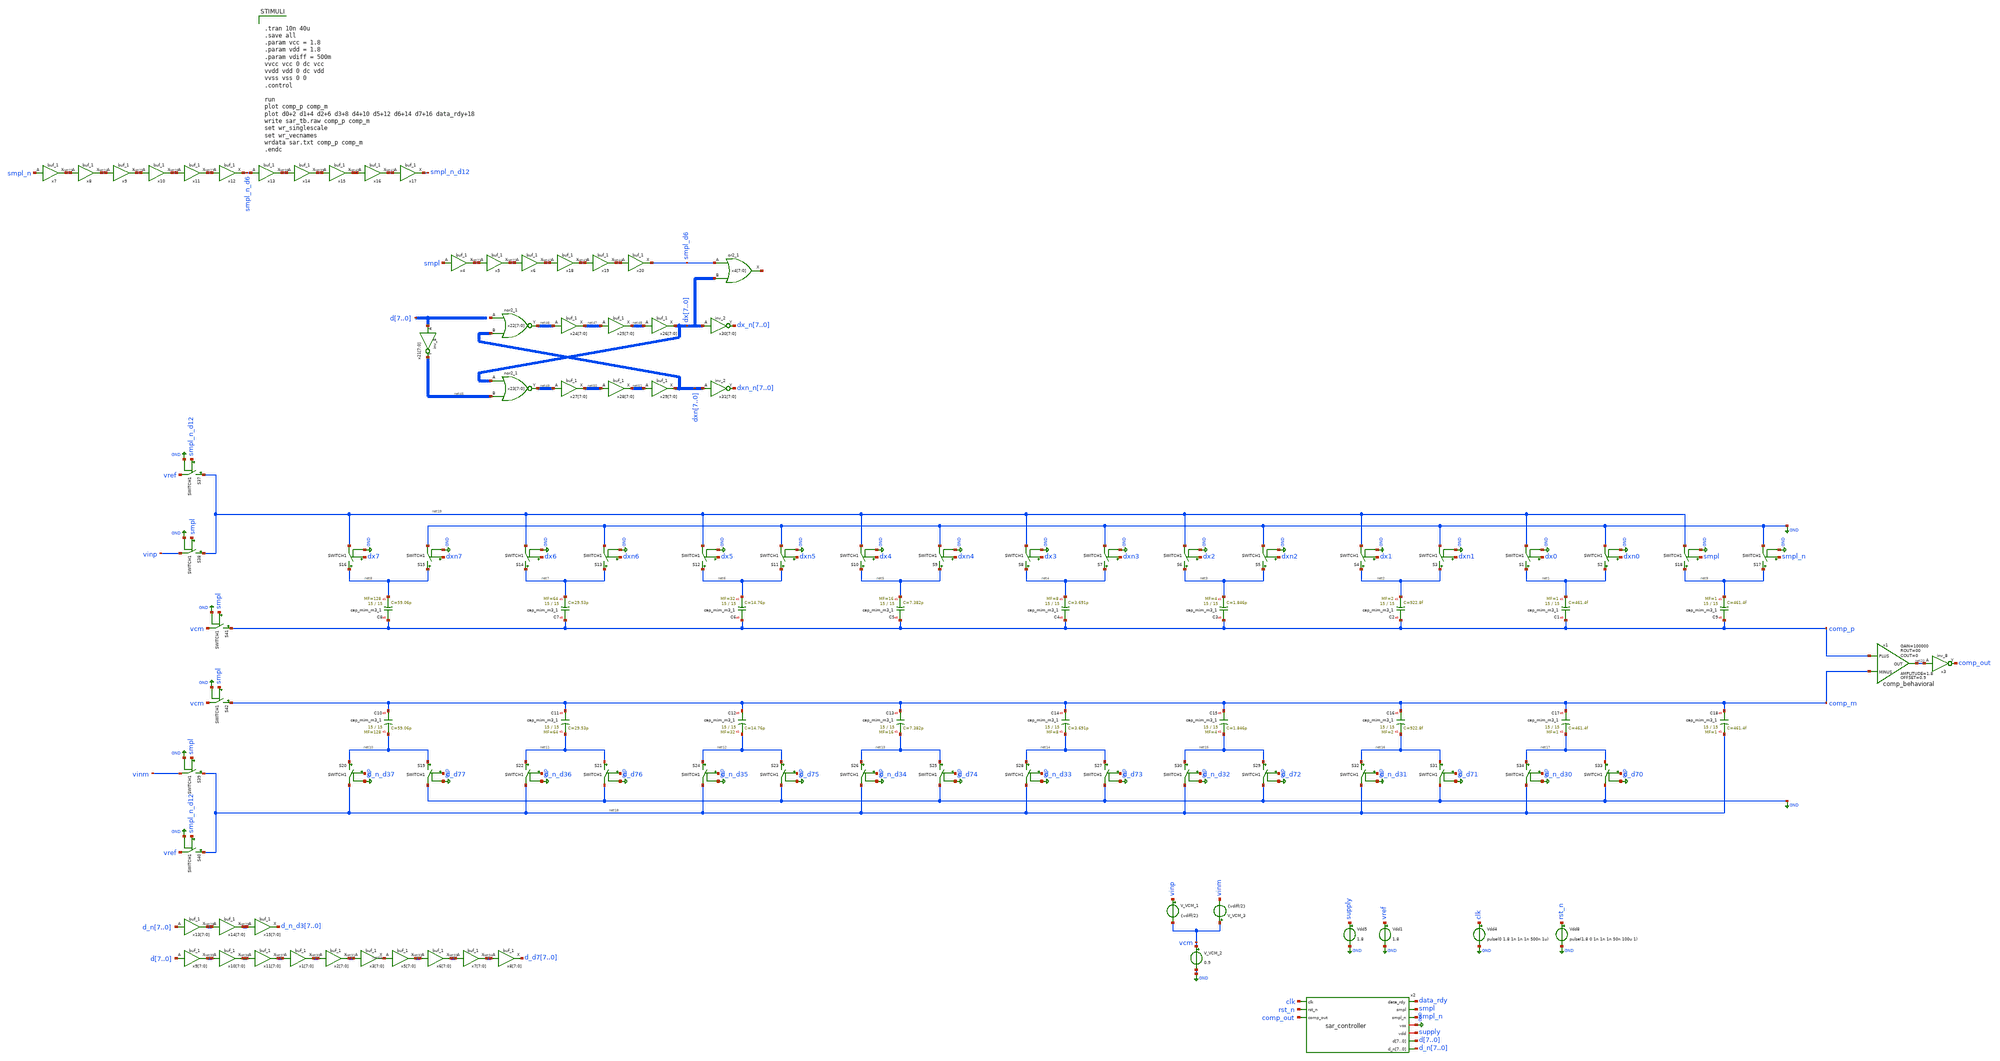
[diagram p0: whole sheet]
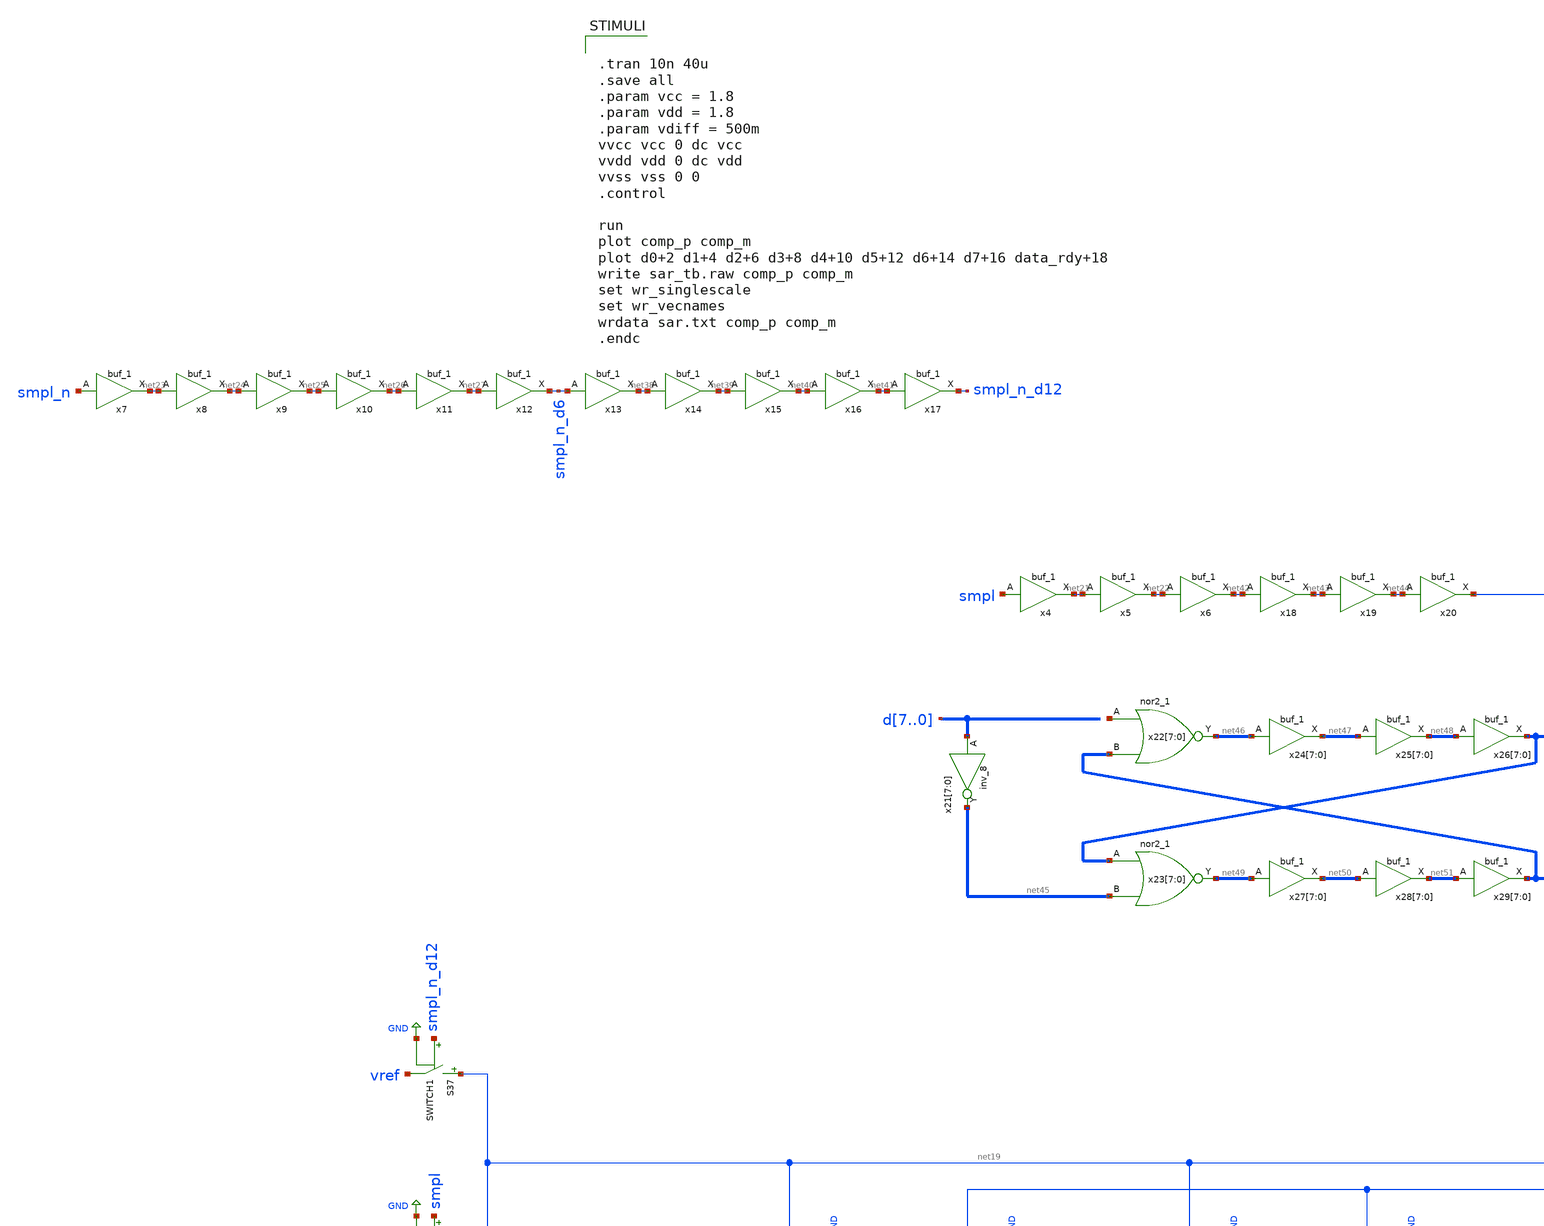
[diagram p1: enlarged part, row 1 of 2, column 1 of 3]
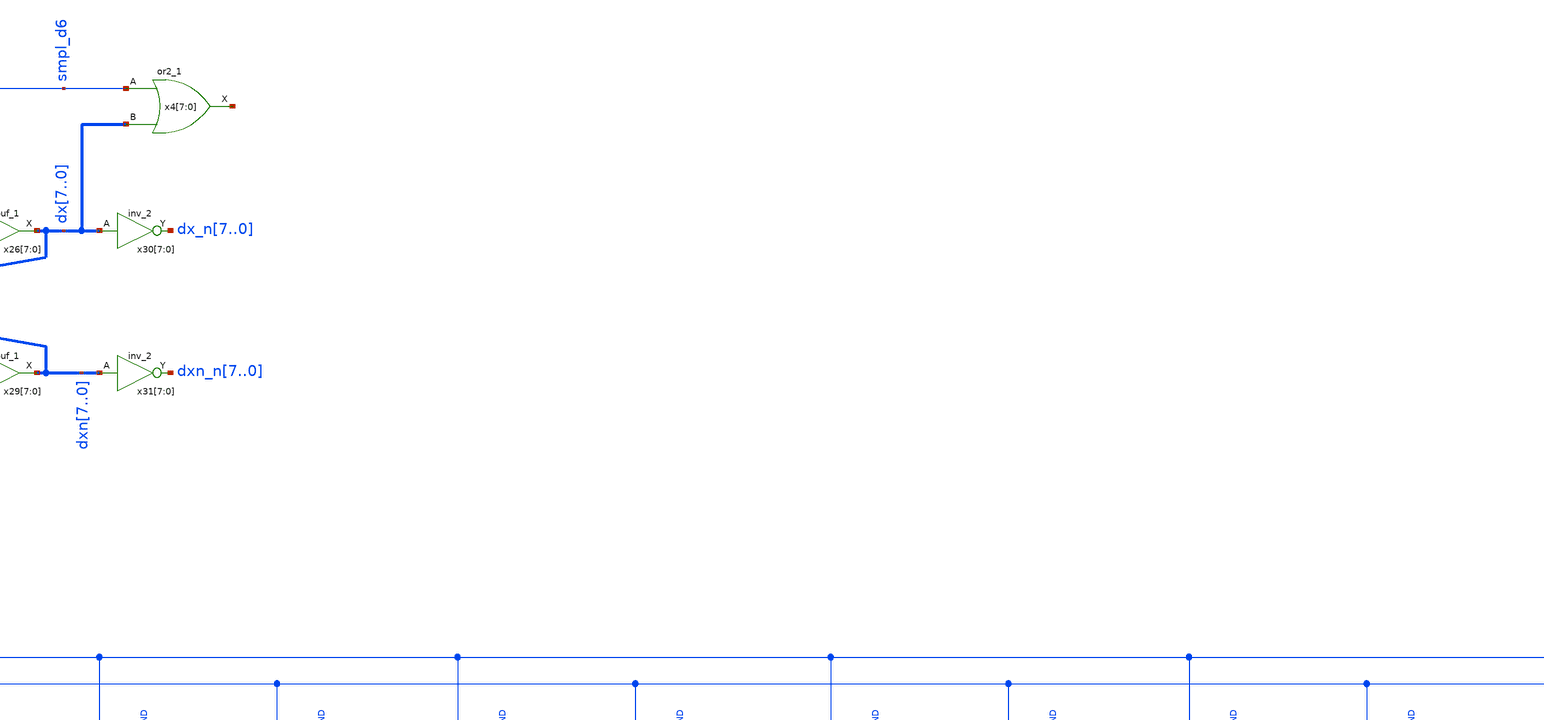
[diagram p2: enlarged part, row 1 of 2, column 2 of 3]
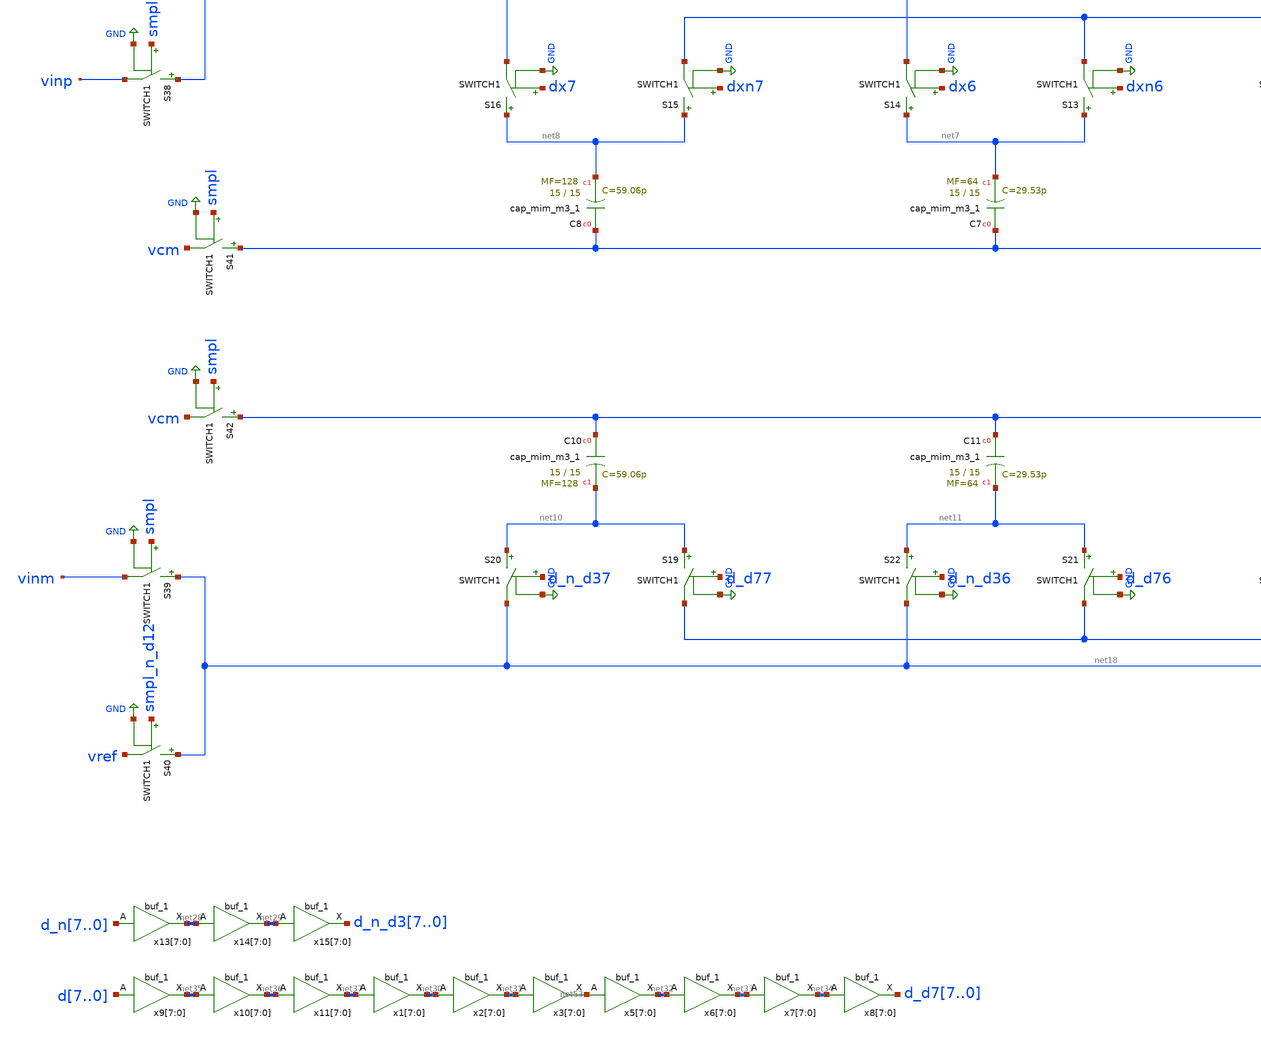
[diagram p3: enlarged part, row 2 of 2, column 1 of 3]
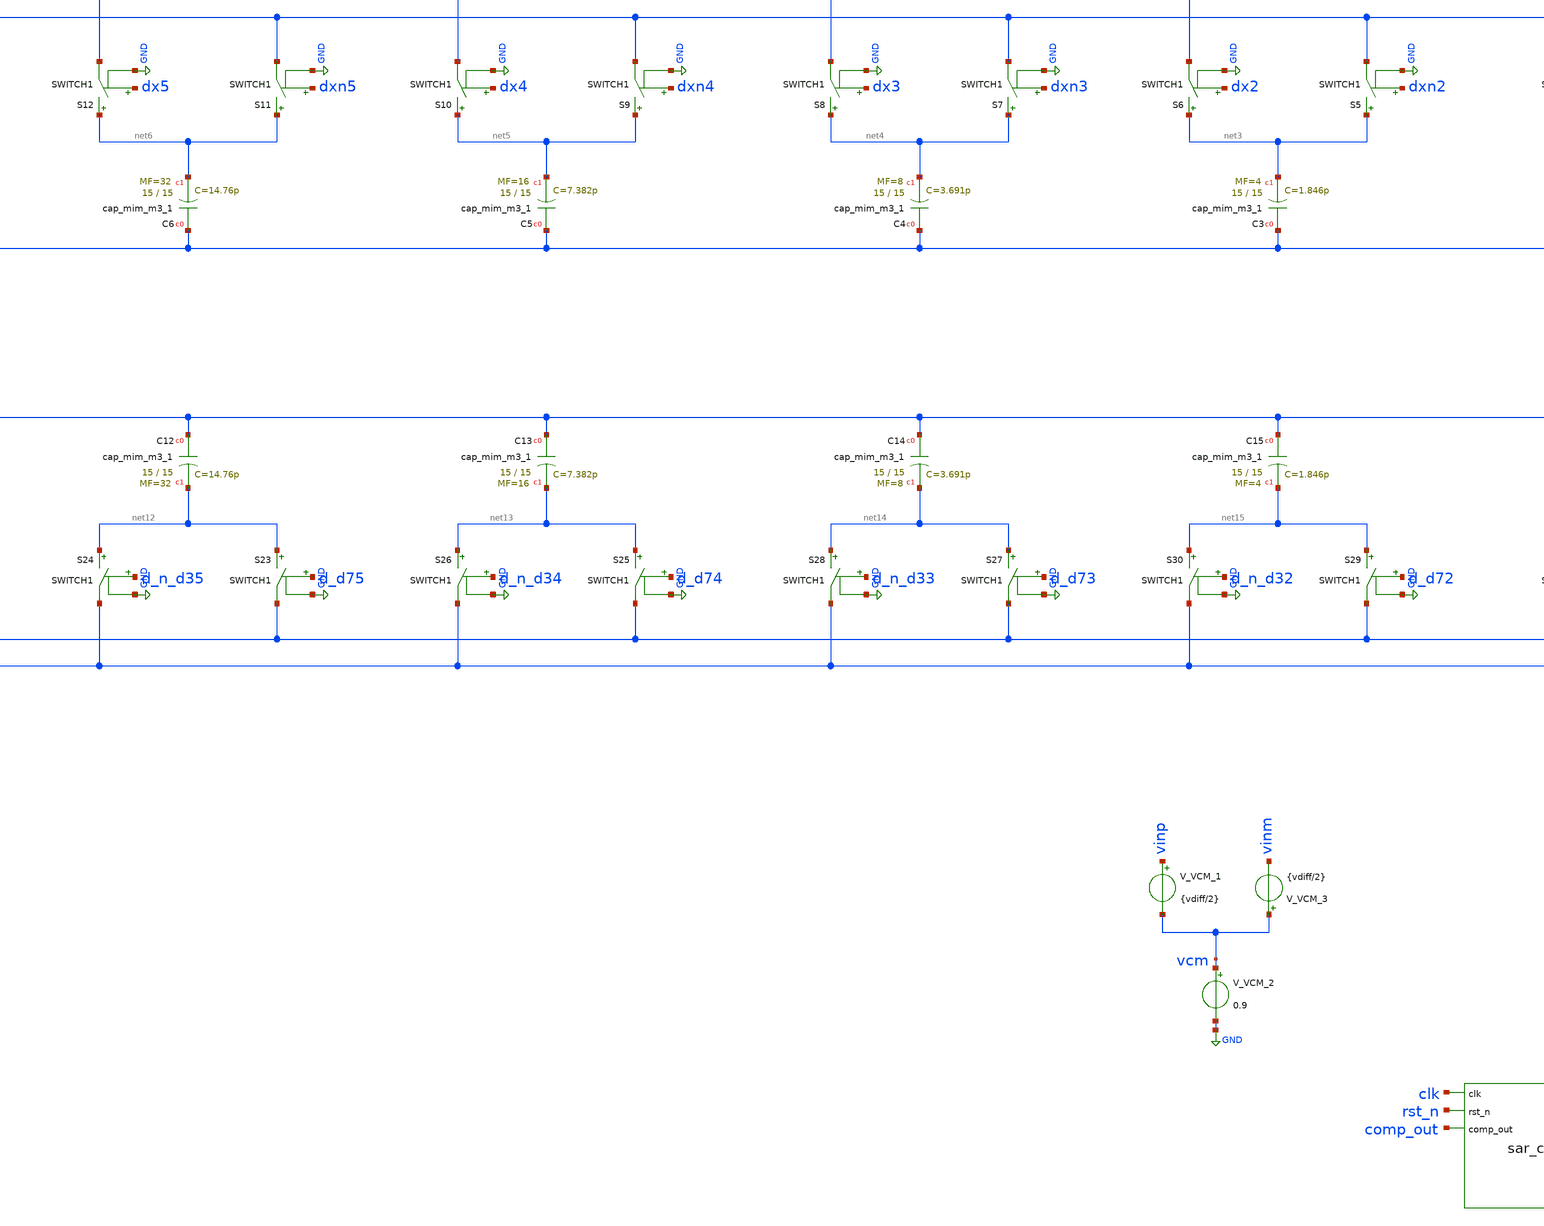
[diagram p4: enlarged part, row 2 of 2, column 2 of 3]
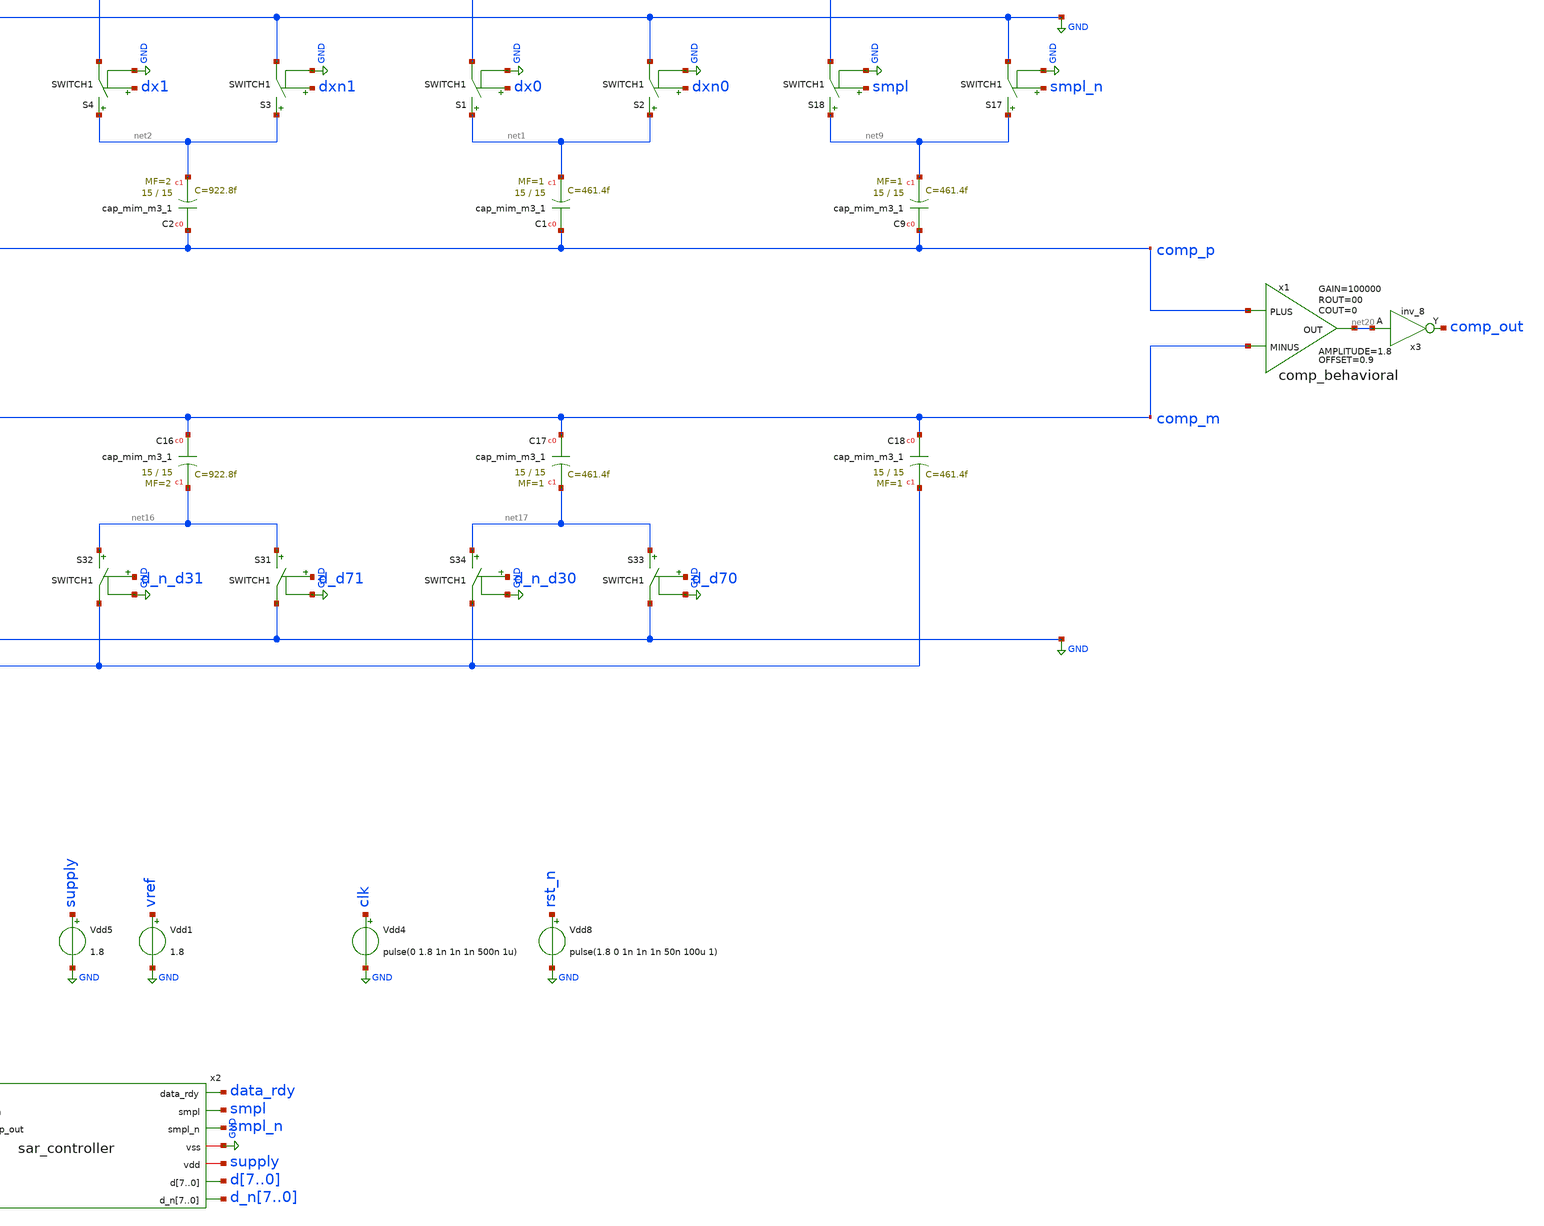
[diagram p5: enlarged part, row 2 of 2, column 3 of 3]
** sch_path: top/untitled-4.sch
.lib $::SKYWATER_MODELS/sky130.lib.spice tt
.include $::SKYWATER_STDCELLS/sky130_fd_sc_hd.spice

**.subckt untitled-4
XC1 comp_p net1 sky130_fd_pr__cap_mim_m3_1 W=15 L=15 MF=1 m=1
S2 net1 GND dxn0 GND SWITCH1
S1 net1 net19 dx0 GND SWITCH1
XC2 comp_p net2 sky130_fd_pr__cap_mim_m3_1 W=15 L=15 MF=2 m=2
S3 net2 GND dxn1 GND SWITCH1
S4 net2 net19 dx1 GND SWITCH1
XC3 comp_p net3 sky130_fd_pr__cap_mim_m3_1 W=15 L=15 MF=4 m=4
S5 net3 GND dxn2 GND SWITCH1
S6 net3 net19 dx2 GND SWITCH1
XC4 comp_p net4 sky130_fd_pr__cap_mim_m3_1 W=15 L=15 MF=8 m=8
S7 net4 GND dxn3 GND SWITCH1
S8 net4 net19 dx3 GND SWITCH1
XC5 comp_p net5 sky130_fd_pr__cap_mim_m3_1 W=15 L=15 MF=16 m=16
S9 net5 GND dxn4 GND SWITCH1
S10 net5 net19 dx4 GND SWITCH1
XC6 comp_p net6 sky130_fd_pr__cap_mim_m3_1 W=15 L=15 MF=32 m=32
S11 net6 GND dxn5 GND SWITCH1
S12 net6 net19 dx5 GND SWITCH1
XC7 comp_p net7 sky130_fd_pr__cap_mim_m3_1 W=15 L=15 MF=64 m=64
S13 net7 GND dxn6 GND SWITCH1
S14 net7 net19 dx6 GND SWITCH1
S15 net8 GND dxn7 GND SWITCH1
S16 net8 net19 dx7 GND SWITCH1
XC9 comp_p net9 sky130_fd_pr__cap_mim_m3_1 W=15 L=15 MF=1 m=1
S17 net9 GND smpl_n GND SWITCH1
S18 net9 net19 smpl GND SWITCH1
XC10 comp_m net10 sky130_fd_pr__cap_mim_m3_1 W=15 L=15 MF=128 m=128
S19 net10 GND d_d77 GND SWITCH1
S20 net10 net18 d_n_d37 GND SWITCH1
XC11 comp_m net11 sky130_fd_pr__cap_mim_m3_1 W=15 L=15 MF=64 m=64
S21 net11 GND d_d76 GND SWITCH1
S22 net11 net18 d_n_d36 GND SWITCH1
XC12 comp_m net12 sky130_fd_pr__cap_mim_m3_1 W=15 L=15 MF=32 m=32
S23 net12 GND d_d75 GND SWITCH1
S24 net12 net18 d_n_d35 GND SWITCH1
XC13 comp_m net13 sky130_fd_pr__cap_mim_m3_1 W=15 L=15 MF=16 m=16
S25 net13 GND d_d74 GND SWITCH1
S26 net13 net18 d_n_d34 GND SWITCH1
XC14 comp_m net14 sky130_fd_pr__cap_mim_m3_1 W=15 L=15 MF=8 m=8
S27 net14 GND d_d73 GND SWITCH1
S28 net14 net18 d_n_d33 GND SWITCH1
XC15 comp_m net15 sky130_fd_pr__cap_mim_m3_1 W=15 L=15 MF=4 m=4
S29 net15 GND d_d72 GND SWITCH1
S30 net15 net18 d_n_d32 GND SWITCH1
XC16 comp_m net16 sky130_fd_pr__cap_mim_m3_1 W=15 L=15 MF=2 m=2
S31 net16 GND d_d71 GND SWITCH1
S32 net16 net18 d_n_d31 GND SWITCH1
XC17 comp_m net17 sky130_fd_pr__cap_mim_m3_1 W=15 L=15 MF=1 m=1
S33 net17 GND d_d70 GND SWITCH1
S34 net17 net18 d_n_d30 GND SWITCH1
XC18 comp_m net18 sky130_fd_pr__cap_mim_m3_1 W=15 L=15 MF=1 m=1
S37 net19 vref smpl_n_d12 GND SWITCH1
S39 net18 vinm smpl GND SWITCH1
S40 net18 vref smpl_n_d12 GND SWITCH1
S41 comp_p vcm smpl GND SWITCH1
S42 comp_m vcm smpl GND SWITCH1
Vdd8 rst_n GND pulse(1.8 0 1n 1n 1n 50n 100u 1)
Vdd4 clk GND pulse(0 1.8 1n 1n 1n 500n 1u)
x4[7] smpl_d6 dx7 vss vss vcc vcc net52[7] sky130_fd_sc_hd__or2_1
x4[6] smpl_d6 dx6 vss vss vcc vcc net52[6] sky130_fd_sc_hd__or2_1
x4[5] smpl_d6 dx5 vss vss vcc vcc net52[5] sky130_fd_sc_hd__or2_1
x4[4] smpl_d6 dx4 vss vss vcc vcc net52[4] sky130_fd_sc_hd__or2_1
x4[3] smpl_d6 dx3 vss vss vcc vcc net52[3] sky130_fd_sc_hd__or2_1
x4[2] smpl_d6 dx2 vss vss vcc vcc net52[2] sky130_fd_sc_hd__or2_1
x4[1] smpl_d6 dx1 vss vss vcc vcc net52[1] sky130_fd_sc_hd__or2_1
x4[0] smpl_d6 dx0 vss vss vcc vcc net52[0] sky130_fd_sc_hd__or2_1
Vdd1 vref GND 1.8
S38 net19 vinp smpl GND SWITCH1
XC8 comp_p net8 sky130_fd_pr__cap_mim_m3_1 W=15 L=15 MF=128 m=128
x1 comp_p comp_m net20 comp_behavioral OFFSET=0.9 AMPLITUDE=1.8 GAIN=100000 ROUT=00 COUT=0
x3 net20 vss vss vcc vcc comp_out sky130_fd_sc_hd__inv_8
x2 clk data_rdy smpl rst_n smpl_n comp_out GND supply d7 d6 d5 d4 d3 d2 d1 d0 d_n7 d_n6 d_n5 d_n4
+ d_n3 d_n2 d_n1 d_n0 sar_controller
Vdd5 supply GND 1.8
V_VCM_2 vcm GND 0.9
V_VCM_1 vinp vcm {vdiff/2}
V_VCM_3 vcm vinm {vdiff/2}
x4 smpl vss vss vdd vdd net21 sky130_fd_sc_hd__buf_1
x5 net21 vss vss vdd vdd net22 sky130_fd_sc_hd__buf_1
x6 net22 vss vss vdd vdd net42 sky130_fd_sc_hd__buf_1
x7 smpl_n vss vss vdd vdd net23 sky130_fd_sc_hd__buf_1
x8 net23 vss vss vdd vdd net24 sky130_fd_sc_hd__buf_1
x9 net24 vss vss vdd vdd net25 sky130_fd_sc_hd__buf_1
x10 net25 vss vss vdd vdd net26 sky130_fd_sc_hd__buf_1
x11 net26 vss vss vdd vdd net27 sky130_fd_sc_hd__buf_1
x12 net27 vss vss vdd vdd smpl_n_d6 sky130_fd_sc_hd__buf_1
x13[7] d_n7 vss vss vdd vdd net28[7] sky130_fd_sc_hd__buf_1
x13[6] d_n6 vss vss vdd vdd net28[6] sky130_fd_sc_hd__buf_1
x13[5] d_n5 vss vss vdd vdd net28[5] sky130_fd_sc_hd__buf_1
x13[4] d_n4 vss vss vdd vdd net28[4] sky130_fd_sc_hd__buf_1
x13[3] d_n3 vss vss vdd vdd net28[3] sky130_fd_sc_hd__buf_1
x13[2] d_n2 vss vss vdd vdd net28[2] sky130_fd_sc_hd__buf_1
x13[1] d_n1 vss vss vdd vdd net28[1] sky130_fd_sc_hd__buf_1
x13[0] d_n0 vss vss vdd vdd net28[0] sky130_fd_sc_hd__buf_1
x14[7] net28[7] vss vss vdd vdd net29[7] sky130_fd_sc_hd__buf_1
x14[6] net28[6] vss vss vdd vdd net29[6] sky130_fd_sc_hd__buf_1
x14[5] net28[5] vss vss vdd vdd net29[5] sky130_fd_sc_hd__buf_1
x14[4] net28[4] vss vss vdd vdd net29[4] sky130_fd_sc_hd__buf_1
x14[3] net28[3] vss vss vdd vdd net29[3] sky130_fd_sc_hd__buf_1
x14[2] net28[2] vss vss vdd vdd net29[2] sky130_fd_sc_hd__buf_1
x14[1] net28[1] vss vss vdd vdd net29[1] sky130_fd_sc_hd__buf_1
x14[0] net28[0] vss vss vdd vdd net29[0] sky130_fd_sc_hd__buf_1
x15[7] net29[7] vss vss vdd vdd d_n_d37 sky130_fd_sc_hd__buf_1
x15[6] net29[6] vss vss vdd vdd d_n_d36 sky130_fd_sc_hd__buf_1
x15[5] net29[5] vss vss vdd vdd d_n_d35 sky130_fd_sc_hd__buf_1
x15[4] net29[4] vss vss vdd vdd d_n_d34 sky130_fd_sc_hd__buf_1
x15[3] net29[3] vss vss vdd vdd d_n_d33 sky130_fd_sc_hd__buf_1
x15[2] net29[2] vss vss vdd vdd d_n_d32 sky130_fd_sc_hd__buf_1
x15[1] net29[1] vss vss vdd vdd d_n_d31 sky130_fd_sc_hd__buf_1
x15[0] net29[0] vss vss vdd vdd d_n_d30 sky130_fd_sc_hd__buf_1
x1[7] net37[7] vss vss vdd vdd net30[7] sky130_fd_sc_hd__buf_1
x1[6] net37[6] vss vss vdd vdd net30[6] sky130_fd_sc_hd__buf_1
x1[5] net37[5] vss vss vdd vdd net30[5] sky130_fd_sc_hd__buf_1
x1[4] net37[4] vss vss vdd vdd net30[4] sky130_fd_sc_hd__buf_1
x1[3] net37[3] vss vss vdd vdd net30[3] sky130_fd_sc_hd__buf_1
x1[2] net37[2] vss vss vdd vdd net30[2] sky130_fd_sc_hd__buf_1
x1[1] net37[1] vss vss vdd vdd net30[1] sky130_fd_sc_hd__buf_1
x1[0] net37[0] vss vss vdd vdd net30[0] sky130_fd_sc_hd__buf_1
x2[7] net30[7] vss vss vdd vdd net31[7] sky130_fd_sc_hd__buf_1
x2[6] net30[6] vss vss vdd vdd net31[6] sky130_fd_sc_hd__buf_1
x2[5] net30[5] vss vss vdd vdd net31[5] sky130_fd_sc_hd__buf_1
x2[4] net30[4] vss vss vdd vdd net31[4] sky130_fd_sc_hd__buf_1
x2[3] net30[3] vss vss vdd vdd net31[3] sky130_fd_sc_hd__buf_1
x2[2] net30[2] vss vss vdd vdd net31[2] sky130_fd_sc_hd__buf_1
x2[1] net30[1] vss vss vdd vdd net31[1] sky130_fd_sc_hd__buf_1
x2[0] net30[0] vss vss vdd vdd net31[0] sky130_fd_sc_hd__buf_1
x3[7] net31[7] vss vss vdd vdd net53[7] sky130_fd_sc_hd__buf_1
x3[6] net31[6] vss vss vdd vdd net53[6] sky130_fd_sc_hd__buf_1
x3[5] net31[5] vss vss vdd vdd net53[5] sky130_fd_sc_hd__buf_1
x3[4] net31[4] vss vss vdd vdd net53[4] sky130_fd_sc_hd__buf_1
x3[3] net31[3] vss vss vdd vdd net53[3] sky130_fd_sc_hd__buf_1
x3[2] net31[2] vss vss vdd vdd net53[2] sky130_fd_sc_hd__buf_1
x3[1] net31[1] vss vss vdd vdd net53[1] sky130_fd_sc_hd__buf_1
x3[0] net31[0] vss vss vdd vdd net53[0] sky130_fd_sc_hd__buf_1
x5[7] net53[7] vss vss vdd vdd net32[7] sky130_fd_sc_hd__buf_1
x5[6] net53[6] vss vss vdd vdd net32[6] sky130_fd_sc_hd__buf_1
x5[5] net53[5] vss vss vdd vdd net32[5] sky130_fd_sc_hd__buf_1
x5[4] net53[4] vss vss vdd vdd net32[4] sky130_fd_sc_hd__buf_1
x5[3] net53[3] vss vss vdd vdd net32[3] sky130_fd_sc_hd__buf_1
x5[2] net53[2] vss vss vdd vdd net32[2] sky130_fd_sc_hd__buf_1
x5[1] net53[1] vss vss vdd vdd net32[1] sky130_fd_sc_hd__buf_1
x5[0] net53[0] vss vss vdd vdd net32[0] sky130_fd_sc_hd__buf_1
x6[7] net32[7] vss vss vdd vdd net33[7] sky130_fd_sc_hd__buf_1
x6[6] net32[6] vss vss vdd vdd net33[6] sky130_fd_sc_hd__buf_1
x6[5] net32[5] vss vss vdd vdd net33[5] sky130_fd_sc_hd__buf_1
x6[4] net32[4] vss vss vdd vdd net33[4] sky130_fd_sc_hd__buf_1
x6[3] net32[3] vss vss vdd vdd net33[3] sky130_fd_sc_hd__buf_1
x6[2] net32[2] vss vss vdd vdd net33[2] sky130_fd_sc_hd__buf_1
x6[1] net32[1] vss vss vdd vdd net33[1] sky130_fd_sc_hd__buf_1
x6[0] net32[0] vss vss vdd vdd net33[0] sky130_fd_sc_hd__buf_1
x7[7] net33[7] vss vss vdd vdd net34[7] sky130_fd_sc_hd__buf_1
x7[6] net33[6] vss vss vdd vdd net34[6] sky130_fd_sc_hd__buf_1
x7[5] net33[5] vss vss vdd vdd net34[5] sky130_fd_sc_hd__buf_1
x7[4] net33[4] vss vss vdd vdd net34[4] sky130_fd_sc_hd__buf_1
x7[3] net33[3] vss vss vdd vdd net34[3] sky130_fd_sc_hd__buf_1
x7[2] net33[2] vss vss vdd vdd net34[2] sky130_fd_sc_hd__buf_1
x7[1] net33[1] vss vss vdd vdd net34[1] sky130_fd_sc_hd__buf_1
x7[0] net33[0] vss vss vdd vdd net34[0] sky130_fd_sc_hd__buf_1
x8[7] net34[7] vss vss vdd vdd d_d77 sky130_fd_sc_hd__buf_1
x8[6] net34[6] vss vss vdd vdd d_d76 sky130_fd_sc_hd__buf_1
x8[5] net34[5] vss vss vdd vdd d_d75 sky130_fd_sc_hd__buf_1
x8[4] net34[4] vss vss vdd vdd d_d74 sky130_fd_sc_hd__buf_1
x8[3] net34[3] vss vss vdd vdd d_d73 sky130_fd_sc_hd__buf_1
x8[2] net34[2] vss vss vdd vdd d_d72 sky130_fd_sc_hd__buf_1
x8[1] net34[1] vss vss vdd vdd d_d71 sky130_fd_sc_hd__buf_1
x8[0] net34[0] vss vss vdd vdd d_d70 sky130_fd_sc_hd__buf_1
x9[7] d7 vss vss vdd vdd net35[7] sky130_fd_sc_hd__buf_1
x9[6] d6 vss vss vdd vdd net35[6] sky130_fd_sc_hd__buf_1
x9[5] d5 vss vss vdd vdd net35[5] sky130_fd_sc_hd__buf_1
x9[4] d4 vss vss vdd vdd net35[4] sky130_fd_sc_hd__buf_1
x9[3] d3 vss vss vdd vdd net35[3] sky130_fd_sc_hd__buf_1
x9[2] d2 vss vss vdd vdd net35[2] sky130_fd_sc_hd__buf_1
x9[1] d1 vss vss vdd vdd net35[1] sky130_fd_sc_hd__buf_1
x9[0] d0 vss vss vdd vdd net35[0] sky130_fd_sc_hd__buf_1
x10[7] net35[7] vss vss vdd vdd net36[7] sky130_fd_sc_hd__buf_1
x10[6] net35[6] vss vss vdd vdd net36[6] sky130_fd_sc_hd__buf_1
x10[5] net35[5] vss vss vdd vdd net36[5] sky130_fd_sc_hd__buf_1
x10[4] net35[4] vss vss vdd vdd net36[4] sky130_fd_sc_hd__buf_1
x10[3] net35[3] vss vss vdd vdd net36[3] sky130_fd_sc_hd__buf_1
x10[2] net35[2] vss vss vdd vdd net36[2] sky130_fd_sc_hd__buf_1
x10[1] net35[1] vss vss vdd vdd net36[1] sky130_fd_sc_hd__buf_1
x10[0] net35[0] vss vss vdd vdd net36[0] sky130_fd_sc_hd__buf_1
x11[7] net36[7] vss vss vdd vdd net37[7] sky130_fd_sc_hd__buf_1
x11[6] net36[6] vss vss vdd vdd net37[6] sky130_fd_sc_hd__buf_1
x11[5] net36[5] vss vss vdd vdd net37[5] sky130_fd_sc_hd__buf_1
x11[4] net36[4] vss vss vdd vdd net37[4] sky130_fd_sc_hd__buf_1
x11[3] net36[3] vss vss vdd vdd net37[3] sky130_fd_sc_hd__buf_1
x11[2] net36[2] vss vss vdd vdd net37[2] sky130_fd_sc_hd__buf_1
x11[1] net36[1] vss vss vdd vdd net37[1] sky130_fd_sc_hd__buf_1
x11[0] net36[0] vss vss vdd vdd net37[0] sky130_fd_sc_hd__buf_1
x13 smpl_n_d6 vss vss vdd vdd net38 sky130_fd_sc_hd__buf_1
x14 net38 vss vss vdd vdd net39 sky130_fd_sc_hd__buf_1
x15 net39 vss vss vdd vdd net40 sky130_fd_sc_hd__buf_1
x16 net40 vss vss vdd vdd net41 sky130_fd_sc_hd__buf_1
x17 net41 vss vss vdd vdd smpl_n_d12 sky130_fd_sc_hd__buf_1
x18 net42 vss vss vdd vdd net43 sky130_fd_sc_hd__buf_1
x19 net43 vss vss vdd vdd net44 sky130_fd_sc_hd__buf_1
x20 net44 vss vss vdd vdd smpl_d6 sky130_fd_sc_hd__buf_1
x21[7] d7 vss vss vcc vcc net45[7] sky130_fd_sc_hd__inv_8
x21[6] d6 vss vss vcc vcc net45[6] sky130_fd_sc_hd__inv_8
x21[5] d5 vss vss vcc vcc net45[5] sky130_fd_sc_hd__inv_8
x21[4] d4 vss vss vcc vcc net45[4] sky130_fd_sc_hd__inv_8
x21[3] d3 vss vss vcc vcc net45[3] sky130_fd_sc_hd__inv_8
x21[2] d2 vss vss vcc vcc net45[2] sky130_fd_sc_hd__inv_8
x21[1] d1 vss vss vcc vcc net45[1] sky130_fd_sc_hd__inv_8
x21[0] d0 vss vss vcc vcc net45[0] sky130_fd_sc_hd__inv_8
x22[7] net54[7] dxn7 VGND VNB VPB VPWR net46[7] sky130_fd_sc_hd__nor2_1
x22[6] net54[6] dxn6 VGND VNB VPB VPWR net46[6] sky130_fd_sc_hd__nor2_1
x22[5] net54[5] dxn5 VGND VNB VPB VPWR net46[5] sky130_fd_sc_hd__nor2_1
x22[4] net54[4] dxn4 VGND VNB VPB VPWR net46[4] sky130_fd_sc_hd__nor2_1
x22[3] net54[3] dxn3 VGND VNB VPB VPWR net46[3] sky130_fd_sc_hd__nor2_1
x22[2] net54[2] dxn2 VGND VNB VPB VPWR net46[2] sky130_fd_sc_hd__nor2_1
x22[1] net54[1] dxn1 VGND VNB VPB VPWR net46[1] sky130_fd_sc_hd__nor2_1
x22[0] net54[0] dxn0 VGND VNB VPB VPWR net46[0] sky130_fd_sc_hd__nor2_1
x23[7] dx7 net45[7] VGND VNB VPB VPWR net49[7] sky130_fd_sc_hd__nor2_1
x23[6] dx6 net45[6] VGND VNB VPB VPWR net49[6] sky130_fd_sc_hd__nor2_1
x23[5] dx5 net45[5] VGND VNB VPB VPWR net49[5] sky130_fd_sc_hd__nor2_1
x23[4] dx4 net45[4] VGND VNB VPB VPWR net49[4] sky130_fd_sc_hd__nor2_1
x23[3] dx3 net45[3] VGND VNB VPB VPWR net49[3] sky130_fd_sc_hd__nor2_1
x23[2] dx2 net45[2] VGND VNB VPB VPWR net49[2] sky130_fd_sc_hd__nor2_1
x23[1] dx1 net45[1] VGND VNB VPB VPWR net49[1] sky130_fd_sc_hd__nor2_1
x23[0] dx0 net45[0] VGND VNB VPB VPWR net49[0] sky130_fd_sc_hd__nor2_1
x24[7] net46[7] vss vss vdd vdd net47[7] sky130_fd_sc_hd__buf_1
x24[6] net46[6] vss vss vdd vdd net47[6] sky130_fd_sc_hd__buf_1
x24[5] net46[5] vss vss vdd vdd net47[5] sky130_fd_sc_hd__buf_1
x24[4] net46[4] vss vss vdd vdd net47[4] sky130_fd_sc_hd__buf_1
x24[3] net46[3] vss vss vdd vdd net47[3] sky130_fd_sc_hd__buf_1
x24[2] net46[2] vss vss vdd vdd net47[2] sky130_fd_sc_hd__buf_1
x24[1] net46[1] vss vss vdd vdd net47[1] sky130_fd_sc_hd__buf_1
x24[0] net46[0] vss vss vdd vdd net47[0] sky130_fd_sc_hd__buf_1
x25[7] net47[7] vss vss vdd vdd net48[7] sky130_fd_sc_hd__buf_1
x25[6] net47[6] vss vss vdd vdd net48[6] sky130_fd_sc_hd__buf_1
x25[5] net47[5] vss vss vdd vdd net48[5] sky130_fd_sc_hd__buf_1
x25[4] net47[4] vss vss vdd vdd net48[4] sky130_fd_sc_hd__buf_1
x25[3] net47[3] vss vss vdd vdd net48[3] sky130_fd_sc_hd__buf_1
x25[2] net47[2] vss vss vdd vdd net48[2] sky130_fd_sc_hd__buf_1
x25[1] net47[1] vss vss vdd vdd net48[1] sky130_fd_sc_hd__buf_1
x25[0] net47[0] vss vss vdd vdd net48[0] sky130_fd_sc_hd__buf_1
x26[7] net48[7] vss vss vdd vdd dx7 sky130_fd_sc_hd__buf_1
x26[6] net48[6] vss vss vdd vdd dx6 sky130_fd_sc_hd__buf_1
x26[5] net48[5] vss vss vdd vdd dx5 sky130_fd_sc_hd__buf_1
x26[4] net48[4] vss vss vdd vdd dx4 sky130_fd_sc_hd__buf_1
x26[3] net48[3] vss vss vdd vdd dx3 sky130_fd_sc_hd__buf_1
x26[2] net48[2] vss vss vdd vdd dx2 sky130_fd_sc_hd__buf_1
x26[1] net48[1] vss vss vdd vdd dx1 sky130_fd_sc_hd__buf_1
x26[0] net48[0] vss vss vdd vdd dx0 sky130_fd_sc_hd__buf_1
x27[7] net49[7] vss vss vdd vdd net50[7] sky130_fd_sc_hd__buf_1
x27[6] net49[6] vss vss vdd vdd net50[6] sky130_fd_sc_hd__buf_1
x27[5] net49[5] vss vss vdd vdd net50[5] sky130_fd_sc_hd__buf_1
x27[4] net49[4] vss vss vdd vdd net50[4] sky130_fd_sc_hd__buf_1
x27[3] net49[3] vss vss vdd vdd net50[3] sky130_fd_sc_hd__buf_1
x27[2] net49[2] vss vss vdd vdd net50[2] sky130_fd_sc_hd__buf_1
x27[1] net49[1] vss vss vdd vdd net50[1] sky130_fd_sc_hd__buf_1
x27[0] net49[0] vss vss vdd vdd net50[0] sky130_fd_sc_hd__buf_1
x28[7] net50[7] vss vss vdd vdd net51[7] sky130_fd_sc_hd__buf_1
x28[6] net50[6] vss vss vdd vdd net51[6] sky130_fd_sc_hd__buf_1
x28[5] net50[5] vss vss vdd vdd net51[5] sky130_fd_sc_hd__buf_1
x28[4] net50[4] vss vss vdd vdd net51[4] sky130_fd_sc_hd__buf_1
x28[3] net50[3] vss vss vdd vdd net51[3] sky130_fd_sc_hd__buf_1
x28[2] net50[2] vss vss vdd vdd net51[2] sky130_fd_sc_hd__buf_1
x28[1] net50[1] vss vss vdd vdd net51[1] sky130_fd_sc_hd__buf_1
x28[0] net50[0] vss vss vdd vdd net51[0] sky130_fd_sc_hd__buf_1
x29[7] net51[7] vss vss vdd vdd dxn7 sky130_fd_sc_hd__buf_1
x29[6] net51[6] vss vss vdd vdd dxn6 sky130_fd_sc_hd__buf_1
x29[5] net51[5] vss vss vdd vdd dxn5 sky130_fd_sc_hd__buf_1
x29[4] net51[4] vss vss vdd vdd dxn4 sky130_fd_sc_hd__buf_1
x29[3] net51[3] vss vss vdd vdd dxn3 sky130_fd_sc_hd__buf_1
x29[2] net51[2] vss vss vdd vdd dxn2 sky130_fd_sc_hd__buf_1
x29[1] net51[1] vss vss vdd vdd dxn1 sky130_fd_sc_hd__buf_1
x29[0] net51[0] vss vss vdd vdd dxn0 sky130_fd_sc_hd__buf_1
x30[7] dx7 vss vss vcc vcc dx_n7 sky130_fd_sc_hd__inv_2
x30[6] dx6 vss vss vcc vcc dx_n6 sky130_fd_sc_hd__inv_2
x30[5] dx5 vss vss vcc vcc dx_n5 sky130_fd_sc_hd__inv_2
x30[4] dx4 vss vss vcc vcc dx_n4 sky130_fd_sc_hd__inv_2
x30[3] dx3 vss vss vcc vcc dx_n3 sky130_fd_sc_hd__inv_2
x30[2] dx2 vss vss vcc vcc dx_n2 sky130_fd_sc_hd__inv_2
x30[1] dx1 vss vss vcc vcc dx_n1 sky130_fd_sc_hd__inv_2
x30[0] dx0 vss vss vcc vcc dx_n0 sky130_fd_sc_hd__inv_2
x31[7] dxn7 vss vss vcc vcc dxn_n7 sky130_fd_sc_hd__inv_2
x31[6] dxn6 vss vss vcc vcc dxn_n6 sky130_fd_sc_hd__inv_2
x31[5] dxn5 vss vss vcc vcc dxn_n5 sky130_fd_sc_hd__inv_2
x31[4] dxn4 vss vss vcc vcc dxn_n4 sky130_fd_sc_hd__inv_2
x31[3] dxn3 vss vss vcc vcc dxn_n3 sky130_fd_sc_hd__inv_2
x31[2] dxn2 vss vss vcc vcc dxn_n2 sky130_fd_sc_hd__inv_2
x31[1] dxn1 vss vss vcc vcc dxn_n1 sky130_fd_sc_hd__inv_2
x31[0] dxn0 vss vss vcc vcc dxn_n0 sky130_fd_sc_hd__inv_2
**** begin user architecture code


.tran 10n 40u
.save all
.param vcc = 1.8
.param vdd = 1.8
.param vdiff = 500m
vvcc vcc 0 dc vcc
vvdd vdd 0 dc vdd
vvss vss 0 0
.control

run
plot comp_p comp_m
plot d0+2 d1+4 d2+6 d3+8 d4+10 d5+12 d6+14 d7+16 data_rdy+18
write sar_tb.raw comp_p comp_m
set wr_singlescale
set wr_vecnames
wrdata sar.txt comp_p comp_m
.endc



.model SWITCH1 sw vt=0.9 vh=0 ron=1 roff =100G

**** end user architecture code
**.ends

* expanding   symbol:  /foss/designs/Behavioural module/Behavioural module/comp_behavioral.sym # of
*+ pins=3
** sym_path: Behavioral_model/comp_behavioral.sym
** sch_path: Behavioral_model/comp_behavioral.sch
.subckt comp_behavioral PLUS MINUS OUT  OFFSET=0.9 AMPLITUDE=0.9 GAIN=100000 ROUT=00 COUT=0
*.ipin PLUS
*.ipin MINUS
*.opin OUT
B1 IOUT 0 V = {OFFSET + AMPLITUDE/2*(tanh(V(IPLUS,IMINUS)*GAIN*2/AMPLITUDE))}
V1 IPLUS PLUS 3
V2 IMINUS MINUS 3
R1 OUT IOUT {ROUT} m=1
C3 OUT 0 {COUT} m=1
.ends


* expanding   symbol:  /foss/designs/test/design/sar_controller.sym # of pins=10
** sym_path: test/design/sar_controller.sym
** sch_path: test/design/sar_controller.sch
.subckt sar_controller clk data_rdy smpl rst_n smpl_n comp_out vss vdd d7 d6 d5 d4 d3 d2 d1 d0 d_n7
+ d_n6 d_n5 d_n4 d_n3 d_n2 d_n1 d_n0
*.ipin rst_n
*.opin data_rdy
*.ipin clk
*.opin smpl
*.ipin comp_out
*.iopin vss
*.iopin vdd
*.opin d7,d6,d5,d4,d3,d2,d1,d0
*.opin d_n7,d_n6,d_n5,d_n4,d_n3,d_n2,d_n1,d_n0
*.opin smpl_n
x26 net2 net21 net22 net9 vss vss vdd vdd net1 net25 sky130_fd_sc_hd__dfbbp_1
x5 net19 net23 net20 vss vss vdd vdd cnv_7 net9 sky130_fd_sc_hd__dfrbp_1
* noconn #net33
x24 net19 net8 net20 vss vss vdd vdd net23 net24 sky130_fd_sc_hd__dfsbp_1
x6 net24 net20 vss vss vdd vdd net22 sky130_fd_sc_hd__and2_4
x1 net19 cnv_7 net20 vss vss vdd vdd cnv_6 net12 sky130_fd_sc_hd__dfrbp_1
x2 net19 cnv_6 net20 vss vss vdd vdd cnv_5 net13 sky130_fd_sc_hd__dfrbp_1
x3 net19 cnv_5 net20 vss vss vdd vdd cnv_4 net14 sky130_fd_sc_hd__dfrbp_1
x4 net19 cnv_4 net20 vss vss vdd vdd cnv_3 net15 sky130_fd_sc_hd__dfrbp_1
x7 net19 cnv_3 net20 vss vss vdd vdd cnv_2 net16 sky130_fd_sc_hd__dfrbp_1
x8 net19 cnv_2 net20 vss vss vdd vdd cnv_1 net17 sky130_fd_sc_hd__dfrbp_1
x9 net19 cnv_1 net20 vss vss vdd vdd cnv_0 net18 sky130_fd_sc_hd__dfrbp_1
x10 net19 cnv_0 net20 vss vss vdd vdd net8 net33 sky130_fd_sc_hd__dfrbp_1
x11 vss vss net22 vss vss vdd vdd net11 net34 sky130_fd_sc_hd__dfrbp_1
x12 net10 net21 net22 net12 vss vss vdd vdd net2 net26 sky130_fd_sc_hd__dfbbp_1
x13 net3 net21 net22 net13 vss vss vdd vdd net10 net27 sky130_fd_sc_hd__dfbbp_1
x14 net4 net21 net22 net14 vss vss vdd vdd net3 net28 sky130_fd_sc_hd__dfbbp_1
x15 net5 net21 net22 net15 vss vss vdd vdd net4 net29 sky130_fd_sc_hd__dfbbp_1
x16 net6 net21 net22 net16 vss vss vdd vdd net5 net30 sky130_fd_sc_hd__dfbbp_1
x17 net7 net21 net22 net17 vss vss vdd vdd net6 net31 sky130_fd_sc_hd__dfbbp_1
x18 net11 net21 net22 net18 vss vss vdd vdd net7 net32 sky130_fd_sc_hd__dfbbp_1
* noconn #net34
x19 net1 vss vss vdd vdd d7 sky130_fd_sc_hd__buf_2
x20 net25 vss vss vdd vdd d_n7 sky130_fd_sc_hd__buf_2
x21 net2 vss vss vdd vdd d6 sky130_fd_sc_hd__buf_2
x22 net26 vss vss vdd vdd d_n6 sky130_fd_sc_hd__buf_2
x23 net10 vss vss vdd vdd d5 sky130_fd_sc_hd__buf_2
x25 net27 vss vss vdd vdd d_n5 sky130_fd_sc_hd__buf_2
x27 net3 vss vss vdd vdd d4 sky130_fd_sc_hd__buf_2
x28 net28 vss vss vdd vdd d_n4 sky130_fd_sc_hd__buf_2
x29 net4 vss vss vdd vdd d3 sky130_fd_sc_hd__buf_2
x30 net29 vss vss vdd vdd d_n3 sky130_fd_sc_hd__buf_2
x31 net5 vss vss vdd vdd d2 sky130_fd_sc_hd__buf_2
x32 net30 vss vss vdd vdd d_n2 sky130_fd_sc_hd__buf_2
x33 net6 vss vss vdd vdd d1 sky130_fd_sc_hd__buf_2
x34 net31 vss vss vdd vdd d_n1 sky130_fd_sc_hd__buf_2
x35 net7 vss vss vdd vdd d0 sky130_fd_sc_hd__buf_2
x36 net32 vss vss vdd vdd d_n0 sky130_fd_sc_hd__buf_2
x37 net23 vss vss vdd vdd smpl sky130_fd_sc_hd__buf_2
x38 net24 vss vss vdd vdd smpl_n sky130_fd_sc_hd__buf_2
x39 net8 vss vss vdd vdd data_rdy sky130_fd_sc_hd__buf_2
x40 comp_out vss vss vdd vdd net21 sky130_fd_sc_hd__buf_4
x41 rst_n vss vss vdd vdd net20 sky130_fd_sc_hd__buf_4
x42 clk vss vss vdd vdd net19 sky130_fd_sc_hd__buf_4
.ends

.GLOBAL GND
.end
